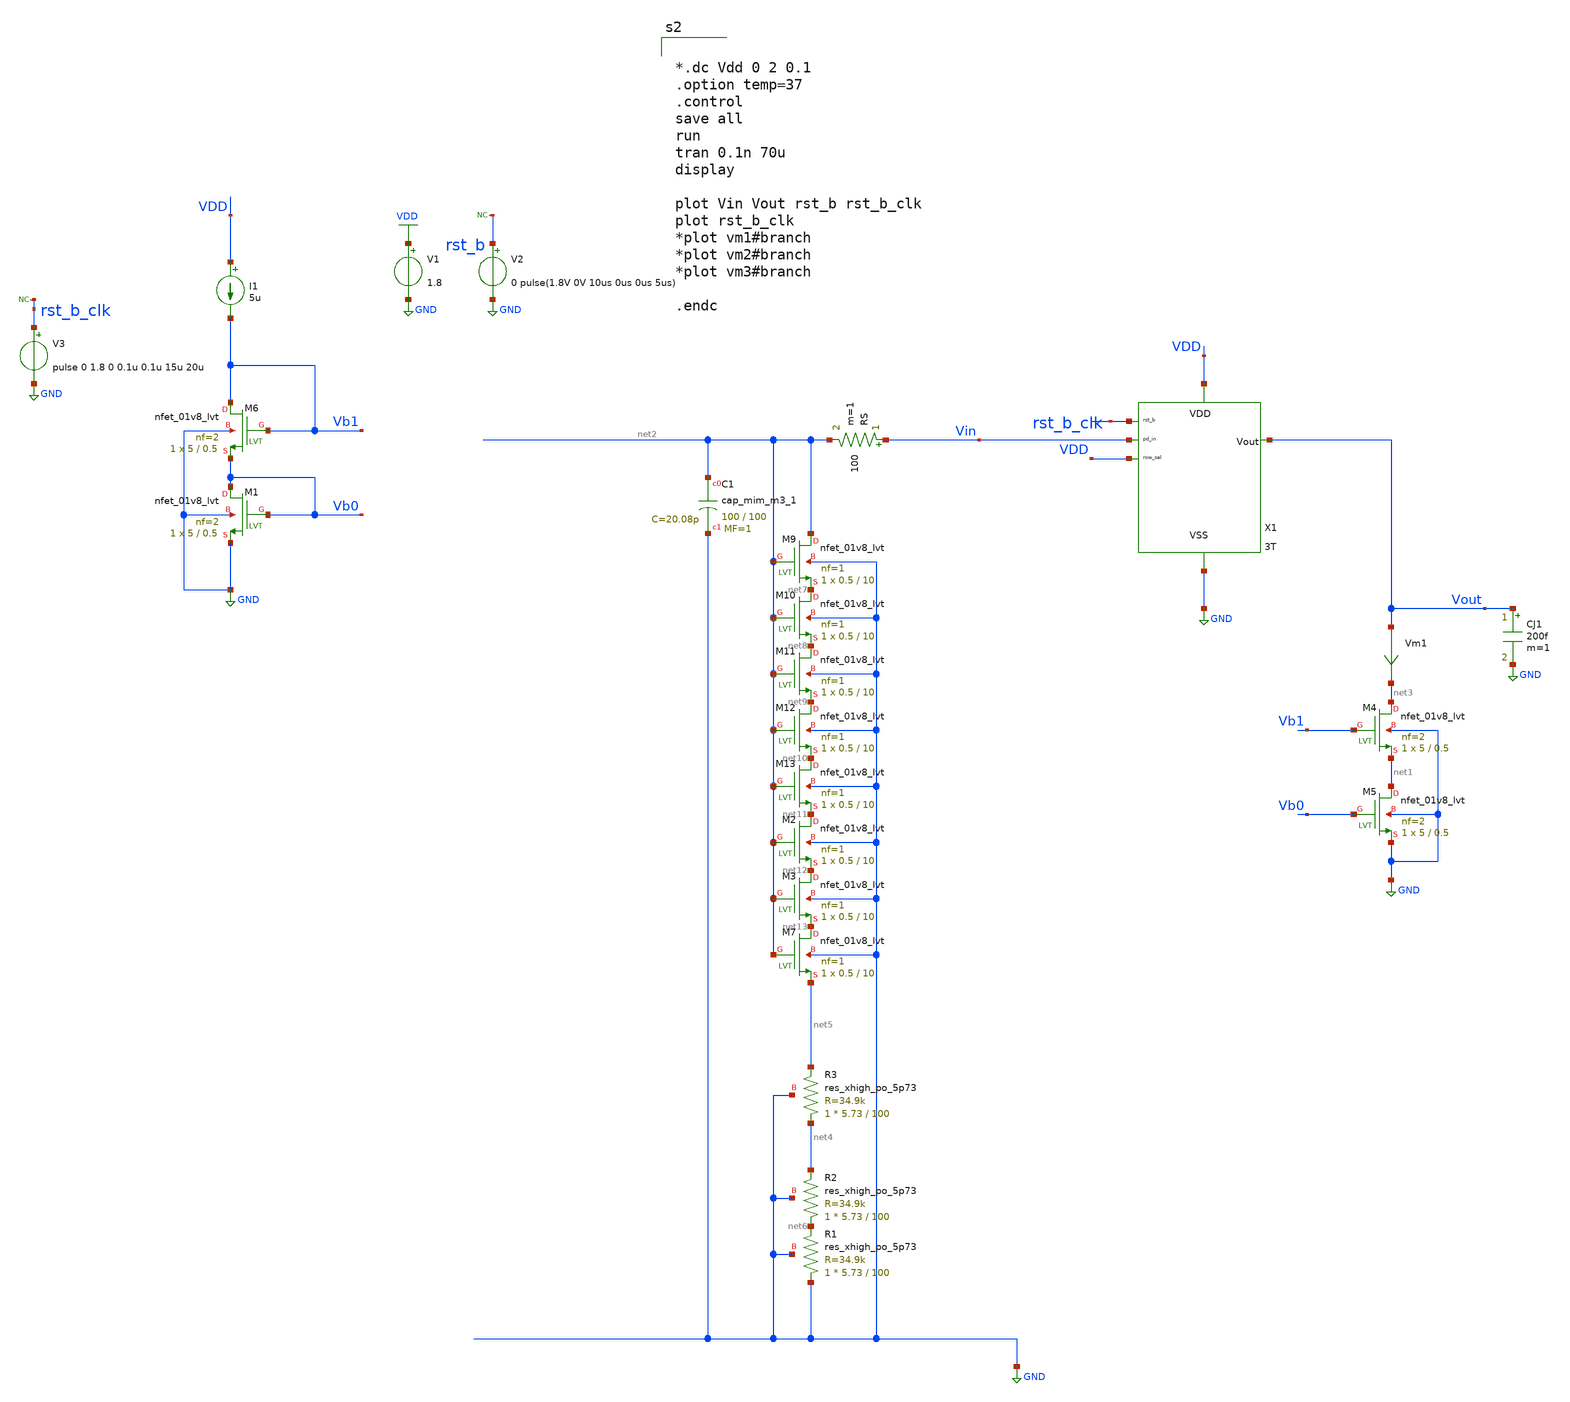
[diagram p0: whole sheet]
** sch_path: xschem/cmos_imager/tb_pixel_real_rc.sch
**.subckt tb_pixel_real_rc
XM4 net3 Vb1 net1 GND sky130_fd_pr__nfet_01v8_lvt L=0.5 W=5 nf=2 ad='int((nf+1)/2) * W/nf * 0.29' as='int((nf+2)/2) * W/nf * 0.29'
+ pd='2*int((nf+1)/2) * (W/nf + 0.29)' ps='2*int((nf+2)/2) * (W/nf + 0.29)' nrd='0.29 / W' nrs='0.29 / W'
+ sa=0 sb=0 sd=0 mult=1 m=1
XM5 net1 Vb0 GND GND sky130_fd_pr__nfet_01v8_lvt L=0.5 W=5 nf=2 ad='int((nf+1)/2) * W/nf * 0.29' as='int((nf+2)/2) * W/nf * 0.29'
+ pd='2*int((nf+1)/2) * (W/nf + 0.29)' ps='2*int((nf+2)/2) * (W/nf + 0.29)' nrd='0.29 / W' nrs='0.29 / W'
+ sa=0 sb=0 sd=0 mult=1 m=1
RS Vin net2 100 m=1
XM6 Vb1 Vb1 Vb0 GND sky130_fd_pr__nfet_01v8_lvt L=0.5 W=5 nf=2 ad='int((nf+1)/2) * W/nf * 0.29' as='int((nf+2)/2) * W/nf * 0.29'
+ pd='2*int((nf+1)/2) * (W/nf + 0.29)' ps='2*int((nf+2)/2) * (W/nf + 0.29)' nrd='0.29 / W' nrs='0.29 / W'
+ sa=0 sb=0 sd=0 mult=1 m=1
XM1 Vb0 Vb0 GND GND sky130_fd_pr__nfet_01v8_lvt L=0.5 W=5 nf=2 ad='int((nf+1)/2) * W/nf * 0.29' as='int((nf+2)/2) * W/nf * 0.29'
+ pd='2*int((nf+1)/2) * (W/nf + 0.29)' ps='2*int((nf+2)/2) * (W/nf + 0.29)' nrd='0.29 / W' nrs='0.29 / W'
+ sa=0 sb=0 sd=0 mult=1 m=1
I1 VDD Vb1 5u
V1 VDD GND 1.8
Vm1 Vout net3 0
.save i(vm1)
V2 rst_b GND 0 pulse(1.8V 0V 10us 0us 0us 5us)
CJ1 Vout GND 200f m=1
X1 VDD Vin rst_b_clk VDD GND Vout 3T
XC1 net2 GND sky130_fd_pr__cap_mim_m3_1 W=100 L=100 MF=1 m=1
XR1 GND net6 GND sky130_fd_pr__res_xhigh_po_5p73 L=100 mult=1 m=1
XR2 net6 net4 GND sky130_fd_pr__res_xhigh_po_5p73 L=100 mult=1 m=1
XM9 net2 net2 net7 GND sky130_fd_pr__nfet_01v8_lvt L=10 W=0.5 nf=1 ad='int((nf+1)/2) * W/nf * 0.29' as='int((nf+2)/2) * W/nf * 0.29'
+ pd='2*int((nf+1)/2) * (W/nf + 0.29)' ps='2*int((nf+2)/2) * (W/nf + 0.29)' nrd='0.29 / W' nrs='0.29 / W'
+ sa=0 sb=0 sd=0 mult=1 m=1
XM10 net7 net2 net8 GND sky130_fd_pr__nfet_01v8_lvt L=10 W=0.5 nf=1 ad='int((nf+1)/2) * W/nf * 0.29'
+ as='int((nf+2)/2) * W/nf * 0.29' pd='2*int((nf+1)/2) * (W/nf + 0.29)' ps='2*int((nf+2)/2) * (W/nf + 0.29)'
+ nrd='0.29 / W' nrs='0.29 / W' sa=0 sb=0 sd=0 mult=1 m=1
XM11 net8 net2 net9 GND sky130_fd_pr__nfet_01v8_lvt L=10 W=0.5 nf=1 ad='int((nf+1)/2) * W/nf * 0.29'
+ as='int((nf+2)/2) * W/nf * 0.29' pd='2*int((nf+1)/2) * (W/nf + 0.29)' ps='2*int((nf+2)/2) * (W/nf + 0.29)'
+ nrd='0.29 / W' nrs='0.29 / W' sa=0 sb=0 sd=0 mult=1 m=1
XM12 net9 net2 net10 GND sky130_fd_pr__nfet_01v8_lvt L=10 W=0.5 nf=1 ad='int((nf+1)/2) * W/nf * 0.29'
+ as='int((nf+2)/2) * W/nf * 0.29' pd='2*int((nf+1)/2) * (W/nf + 0.29)' ps='2*int((nf+2)/2) * (W/nf + 0.29)'
+ nrd='0.29 / W' nrs='0.29 / W' sa=0 sb=0 sd=0 mult=1 m=1
XM13 net10 net2 net11 GND sky130_fd_pr__nfet_01v8_lvt L=10 W=0.5 nf=1 ad='int((nf+1)/2) * W/nf * 0.29'
+ as='int((nf+2)/2) * W/nf * 0.29' pd='2*int((nf+1)/2) * (W/nf + 0.29)' ps='2*int((nf+2)/2) * (W/nf + 0.29)'
+ nrd='0.29 / W' nrs='0.29 / W' sa=0 sb=0 sd=0 mult=1 m=1
XM2 net11 net2 net12 GND sky130_fd_pr__nfet_01v8_lvt L=10 W=0.5 nf=1 ad='int((nf+1)/2) * W/nf * 0.29'
+ as='int((nf+2)/2) * W/nf * 0.29' pd='2*int((nf+1)/2) * (W/nf + 0.29)' ps='2*int((nf+2)/2) * (W/nf + 0.29)'
+ nrd='0.29 / W' nrs='0.29 / W' sa=0 sb=0 sd=0 mult=1 m=1
XM3 net12 net2 net13 GND sky130_fd_pr__nfet_01v8_lvt L=10 W=0.5 nf=1 ad='int((nf+1)/2) * W/nf * 0.29'
+ as='int((nf+2)/2) * W/nf * 0.29' pd='2*int((nf+1)/2) * (W/nf + 0.29)' ps='2*int((nf+2)/2) * (W/nf + 0.29)'
+ nrd='0.29 / W' nrs='0.29 / W' sa=0 sb=0 sd=0 mult=1 m=1
XM7 net13 net2 net5 GND sky130_fd_pr__nfet_01v8_lvt L=10 W=0.5 nf=1 ad='int((nf+1)/2) * W/nf * 0.29'
+ as='int((nf+2)/2) * W/nf * 0.29' pd='2*int((nf+1)/2) * (W/nf + 0.29)' ps='2*int((nf+2)/2) * (W/nf + 0.29)'
+ nrd='0.29 / W' nrs='0.29 / W' sa=0 sb=0 sd=0 mult=1 m=1
V3 rst_b_clk GND pulse 0 1.8 0 0.1u 0.1u 15u 20u
* noconn rst_b_clk
* noconn rst_b
XR3 net4 net5 GND sky130_fd_pr__res_xhigh_po_5p73 L=100 mult=1 m=1
**** begin user architecture code

** opencircuitdesign pdks install
.lib $::SKYWATER_MODELS/sky130.lib.spice tt




*.dc Vdd 0 2 0.1
.option temp=37
.control
save all
run
tran 0.1n 70u
display

plot Vin Vout rst_b rst_b_clk
plot rst_b_clk
*plot vm1#branch
*plot vm2#branch
*plot vm3#branch

.endc


**** end user architecture code
**.ends

* expanding   symbol:  cmos_imager/3T.sym # of pins=6
** sym_path: xschem/cmos_imager/3T.sym
** sch_path: xschem/cmos_imager/3T.sch
.subckt 3T row_sel pd_in rst_b VDD VSS Vout
*.opin Vout
*.ipin rst_b
*.ipin pd_in
*.iopin VDD
*.ipin row_sel
*.iopin VSS
XM2 net2 pd_in net1 VSS sky130_fd_pr__nfet_01v8_lvt L=0.5 W=2 nf=1 ad='int((nf+1)/2) * W/nf * 0.29' as='int((nf+2)/2) * W/nf * 0.29'
+ pd='2*int((nf+1)/2) * (W/nf + 0.29)' ps='2*int((nf+2)/2) * (W/nf + 0.29)' nrd='0.29 / W' nrs='0.29 / W'
+ sa=0 sb=0 sd=0 mult=2 m=2
Vm2 net1 Vmid 0
.save i(vm2)
Vm3 VDD net2 0
.save i(vm3)
XM3 Vmid row_sel Vout VSS sky130_fd_pr__nfet_01v8_lvt L=0.5 W=2 nf=1 ad='int((nf+1)/2) * W/nf * 0.29'
+ as='int((nf+2)/2) * W/nf * 0.29' pd='2*int((nf+1)/2) * (W/nf + 0.29)' ps='2*int((nf+2)/2) * (W/nf + 0.29)'
+ nrd='0.29 / W' nrs='0.29 / W' sa=0 sb=0 sd=0 mult=1 m=1
XM20 pd_in rst_b VDD VDD sky130_fd_pr__pfet_01v8 L=0.5 W=2 nf=1 ad='int((nf+1)/2) * W/nf * 0.29' as='int((nf+2)/2) * W/nf * 0.29'
+ pd='2*int((nf+1)/2) * (W/nf + 0.29)' ps='2*int((nf+2)/2) * (W/nf + 0.29)' nrd='0.29 / W' nrs='0.29 / W'
+ sa=0 sb=0 sd=0 mult=1 m=1
.ends

.GLOBAL GND
.GLOBAL VDD
.end
